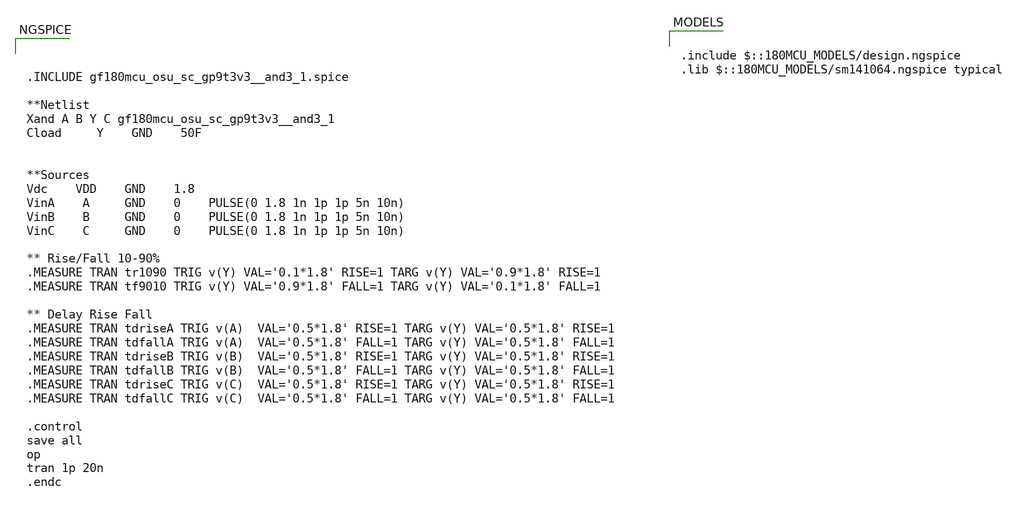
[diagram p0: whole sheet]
** sch_path: xschem/TB_9t3v3_and3_1.sch
**.subckt TB_9t3v3_and3_1
**** begin user architecture code



.INCLUDE gf180mcu_osu_sc_gp9t3v3__and3_1.spice

**Netlist
Xand A B Y C gf180mcu_osu_sc_gp9t3v3__and3_1
Cload 	Y	GND	50F


**Sources
Vdc	VDD	GND	1.8
VinA	A 	GND	0	PULSE(0 1.8 1n 1p 1p 5n 10n)
VinB	B 	GND	0	PULSE(0 1.8 1n 1p 1p 5n 10n)
VinC	C 	GND	0	PULSE(0 1.8 1n 1p 1p 5n 10n)

** Rise/Fall 10-90%
.MEASURE TRAN tr1090 TRIG v(Y) VAL='0.1*1.8' RISE=1 TARG v(Y) VAL='0.9*1.8' RISE=1
.MEASURE TRAN tf9010 TRIG v(Y) VAL='0.9*1.8' FALL=1 TARG v(Y) VAL='0.1*1.8' FALL=1

** Delay Rise Fall
.MEASURE TRAN tdriseA TRIG v(A)  VAL='0.5*1.8' RISE=1 TARG v(Y) VAL='0.5*1.8' RISE=1
.MEASURE TRAN tdfallA TRIG v(A)  VAL='0.5*1.8' FALL=1 TARG v(Y) VAL='0.5*1.8' FALL=1
.MEASURE TRAN tdriseB TRIG v(B)  VAL='0.5*1.8' RISE=1 TARG v(Y) VAL='0.5*1.8' RISE=1
.MEASURE TRAN tdfallB TRIG v(B)  VAL='0.5*1.8' FALL=1 TARG v(Y) VAL='0.5*1.8' FALL=1
.MEASURE TRAN tdriseC TRIG v(C)  VAL='0.5*1.8' RISE=1 TARG v(Y) VAL='0.5*1.8' RISE=1
.MEASURE TRAN tdfallC TRIG v(C)  VAL='0.5*1.8' FALL=1 TARG v(Y) VAL='0.5*1.8' FALL=1

.control
save all
op
tran 1p 20n
.endc



.include $::180MCU_MODELS/design.ngspice
.lib $::180MCU_MODELS/sm141064.ngspice typical

**** end user architecture code
**.ends
.end
